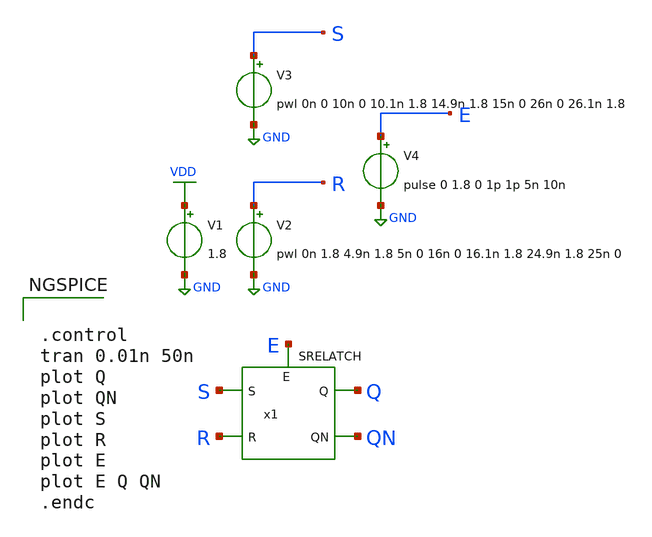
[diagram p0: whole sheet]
** sch_path: current/xschem/test_SRELATACH.sch
**.subckt test_SRELATACH
V2 R GND pwl 0n 1.8 4.9n 1.8 5n 0 16n 0 16.1n 1.8 24.9n 1.8 25n 0
V1 VDD GND 1.8
V3 S GND pwl 0n 0 10n 0 10.1n 1.8 14.9n 1.8 15n 0 26n 0 26.1n 1.8
V4 E GND pulse 0 1.8 0 1p 1p 5n 10n
x1 Q QN S R E VDD GND SRELATCH
**** begin user architecture code

.lib $::SKYWATER_MODELS/sky130.lib.spice tt


**** end user architecture code
**.ends
.GLOBAL VDD
.GLOBAL GND
**** begin user architecture code


.control
tran 0.01n 50n
plot Q
plot QN
plot S
plot R
plot E
plot E Q QN
.endc


**** end user architecture code
.end
